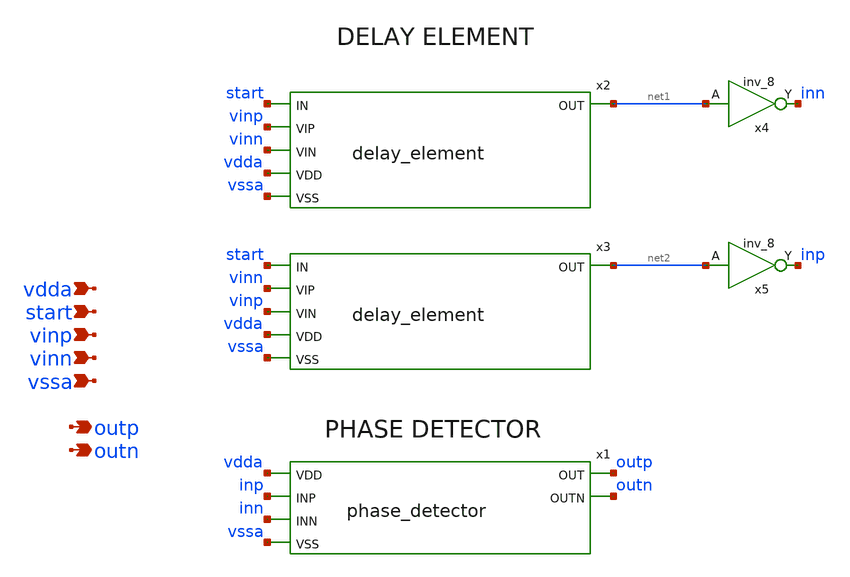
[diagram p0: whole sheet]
** sch_path: xschem/tdc.sch
**.subckt tdc vinn vinp vdda vssa start outp outn
*.ipin vinn
*.ipin vinp
*.ipin vdda
*.ipin vssa
*.ipin start
*.opin outp
*.opin outn
x1 vdda inp inn vssa outp outn phase_detector
x4 net1 vssa vssa vdda vdda inn sky130_fd_sc_hd__inv_8
x5 net2 vssa vssa vdda vdda inp sky130_fd_sc_hd__inv_8
x2 start net1 vinp vinn vdda vssa delay_element
x3 start net2 vinn vinp vdda vssa delay_element
**.ends
.end
